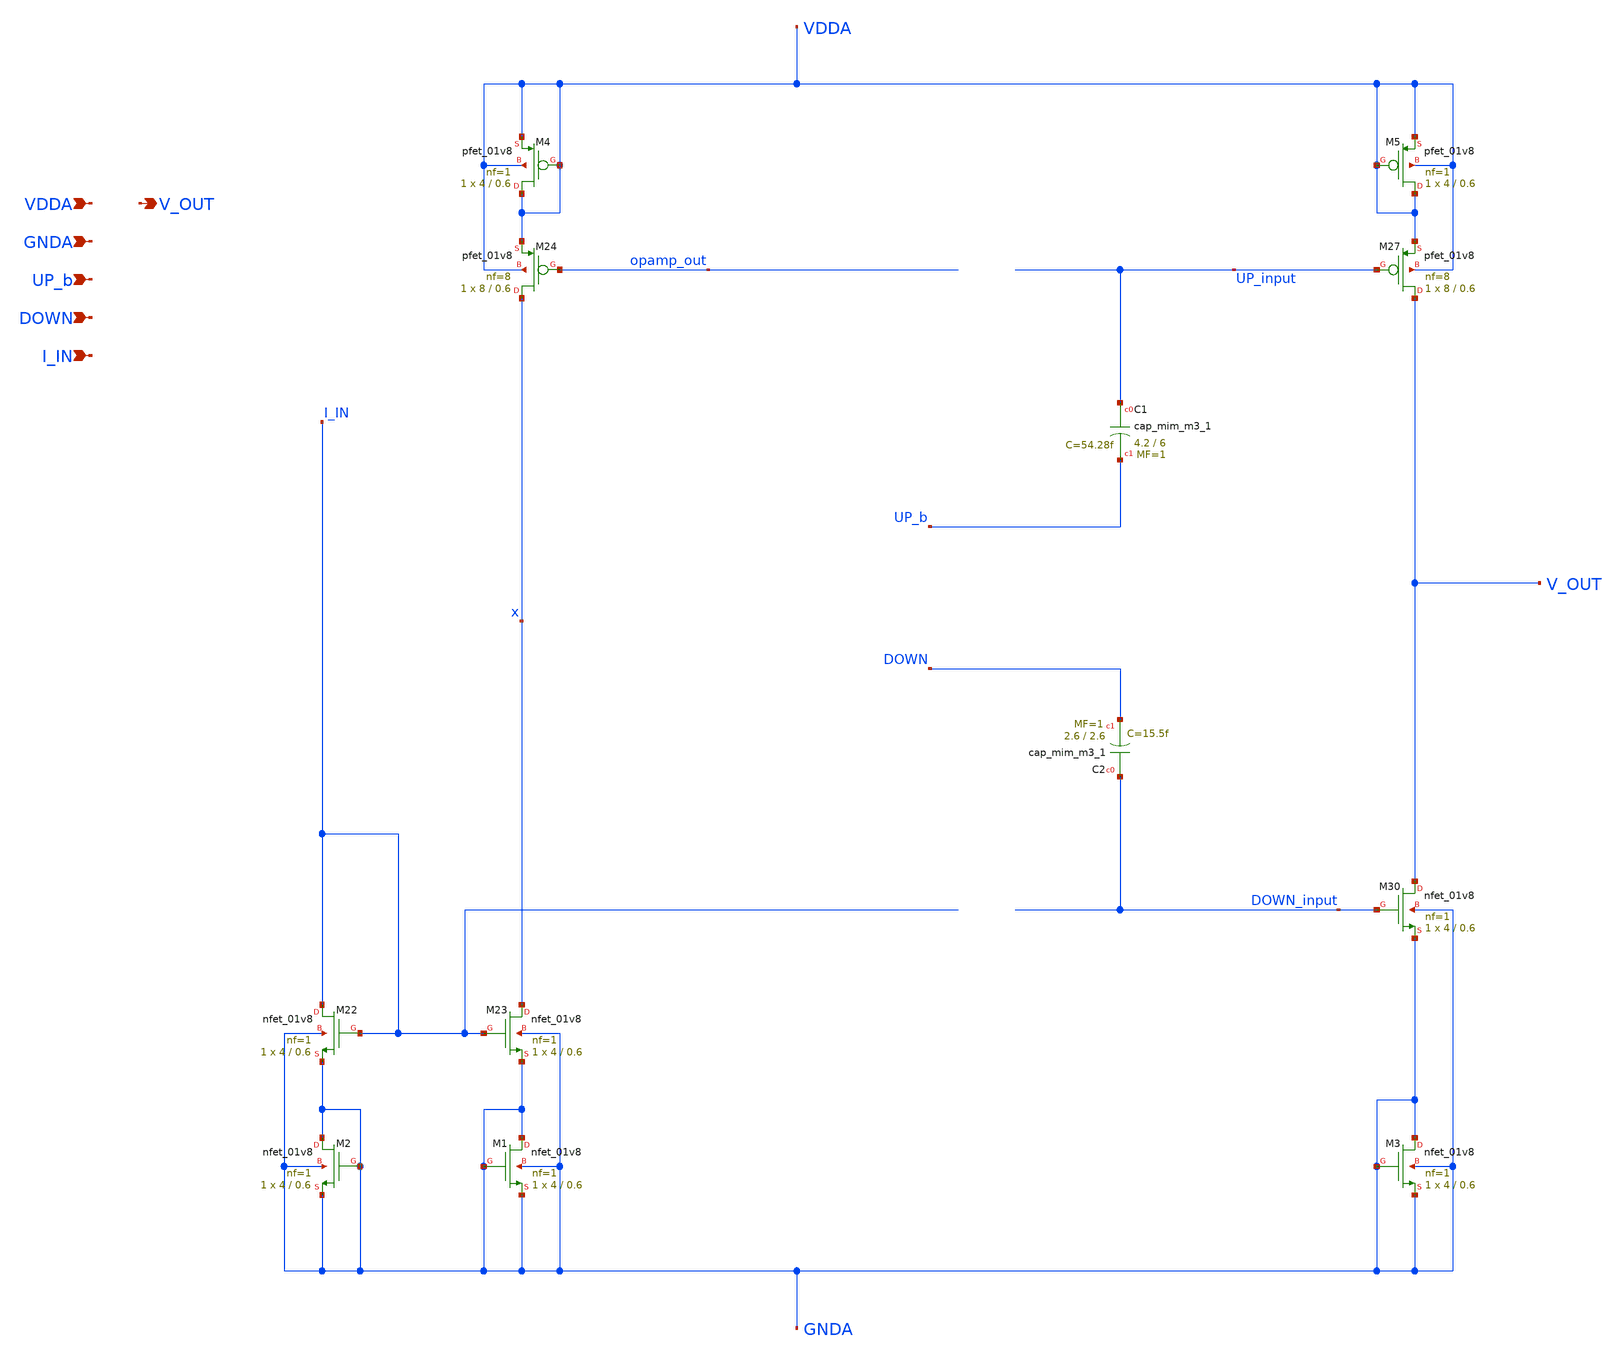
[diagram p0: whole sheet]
** sch_path: projects/pll/charge_pump/xschem_ngspice/charge_pump_xschem_2.sch
**.subckt charge_pump_xschem_2 VDDA V_OUT GNDA UP_b DOWN I_IN
*.ipin VDDA
*.opin V_OUT
*.ipin GNDA
*.ipin UP_b
*.ipin DOWN
*.ipin I_IN
XM22 I_IN I_IN GNDA GNDA sky130_fd_pr__nfet_01v8 L=0.6 W=4 nf=1 ad='int((nf+1)/2) * W/nf * 0.29' as='int((nf+2)/2) * W/nf * 0.29'
+ pd='2*int((nf+1)/2) * (W/nf + 0.29)' ps='2*int((nf+2)/2) * (W/nf + 0.29)' nrd='0.29 / W' nrs='0.29 / W'
+ sa=0 sb=0 sd=0 mult=1 m=1
XM23 x I_IN GNDA GNDA sky130_fd_pr__nfet_01v8 L=0.6 W=4 nf=1 ad='int((nf+1)/2) * W/nf * 0.29' as='int((nf+2)/2) * W/nf * 0.29'
+ pd='2*int((nf+1)/2) * (W/nf + 0.29)' ps='2*int((nf+2)/2) * (W/nf + 0.29)' nrd='0.29 / W' nrs='0.29 / W'
+ sa=0 sb=0 sd=0 mult=1 m=1
XM24 x opamp_out VDDA VDDA sky130_fd_pr__pfet_01v8 L=0.6 W=8 nf=8 ad='int((nf+1)/2) * W/nf * 0.29' as='int((nf+2)/2) * W/nf * 0.29'
+ pd='2*int((nf+1)/2) * (W/nf + 0.29)' ps='2*int((nf+2)/2) * (W/nf + 0.29)' nrd='0.29 / W' nrs='0.29 / W'
+ sa=0 sb=0 sd=0 mult=1 m=1
XM27 V_OUT UP_input VDDA VDDA sky130_fd_pr__pfet_01v8 L=0.6 W=8 nf=8 ad='int((nf+1)/2) * W/nf * 0.29'
+ as='int((nf+2)/2) * W/nf * 0.29' pd='2*int((nf+1)/2) * (W/nf + 0.29)' ps='2*int((nf+2)/2) * (W/nf + 0.29)'
+ nrd='0.29 / W' nrs='0.29 / W' sa=0 sb=0 sd=0 mult=1 m=1
XM30 V_OUT DOWN_input GNDA GNDA sky130_fd_pr__nfet_01v8 L=0.6 W=4 nf=1 ad='int((nf+1)/2) * W/nf * 0.29'
+ as='int((nf+2)/2) * W/nf * 0.29' pd='2*int((nf+1)/2) * (W/nf + 0.29)' ps='2*int((nf+2)/2) * (W/nf + 0.29)'
+ nrd='0.29 / W' nrs='0.29 / W' sa=0 sb=0 sd=0 mult=1 m=1
XC1 UP_input UP_b sky130_fd_pr__cap_mim_m3_1 W=4.2 L=6 MF=1 m=1
XC2 DOWN_input DOWN sky130_fd_pr__cap_mim_m3_1 W=2.6 L=2.6 MF=1 m=1
XM4 VDDA VDDA VDDA VDDA sky130_fd_pr__pfet_01v8 L=0.6 W=4 nf=1 ad='int((nf+1)/2) * W/nf * 0.29' as='int((nf+2)/2) * W/nf * 0.29'
+ pd='2*int((nf+1)/2) * (W/nf + 0.29)' ps='2*int((nf+2)/2) * (W/nf + 0.29)' nrd='0.29 / W' nrs='0.29 / W'
+ sa=0 sb=0 sd=0 mult=1 m=1
XM5 VDDA VDDA VDDA VDDA sky130_fd_pr__pfet_01v8 L=0.6 W=4 nf=1 ad='int((nf+1)/2) * W/nf * 0.29' as='int((nf+2)/2) * W/nf * 0.29'
+ pd='2*int((nf+1)/2) * (W/nf + 0.29)' ps='2*int((nf+2)/2) * (W/nf + 0.29)' nrd='0.29 / W' nrs='0.29 / W'
+ sa=0 sb=0 sd=0 mult=1 m=1
XM1 GNDA GNDA GNDA GNDA sky130_fd_pr__nfet_01v8 L=0.6 W=4 nf=1 ad='int((nf+1)/2) * W/nf * 0.29' as='int((nf+2)/2) * W/nf * 0.29'
+ pd='2*int((nf+1)/2) * (W/nf + 0.29)' ps='2*int((nf+2)/2) * (W/nf + 0.29)' nrd='0.29 / W' nrs='0.29 / W'
+ sa=0 sb=0 sd=0 mult=1 m=1
XM2 GNDA GNDA GNDA GNDA sky130_fd_pr__nfet_01v8 L=0.6 W=4 nf=1 ad='int((nf+1)/2) * W/nf * 0.29' as='int((nf+2)/2) * W/nf * 0.29'
+ pd='2*int((nf+1)/2) * (W/nf + 0.29)' ps='2*int((nf+2)/2) * (W/nf + 0.29)' nrd='0.29 / W' nrs='0.29 / W'
+ sa=0 sb=0 sd=0 mult=1 m=1
XM3 GNDA GNDA GNDA GNDA sky130_fd_pr__nfet_01v8 L=0.6 W=4 nf=1 ad='int((nf+1)/2) * W/nf * 0.29' as='int((nf+2)/2) * W/nf * 0.29'
+ pd='2*int((nf+1)/2) * (W/nf + 0.29)' ps='2*int((nf+2)/2) * (W/nf + 0.29)' nrd='0.29 / W' nrs='0.29 / W'
+ sa=0 sb=0 sd=0 mult=1 m=1
**.ends
.end
